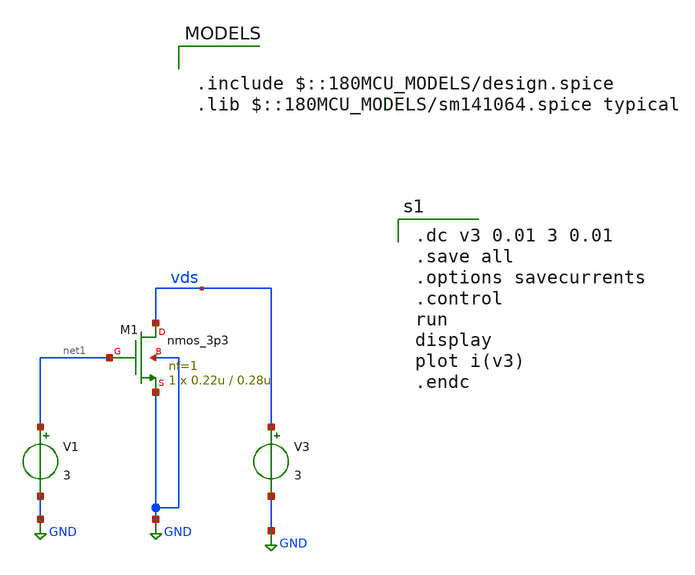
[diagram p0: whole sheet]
** sch_path: xschem/untitled-1.sch
**.subckt untitled-1
XM1 vds net1 GND GND nmos_3p3 L=0.28u W=0.22u nf=1 ad='int((nf+1)/2) * W/nf * 0.18u' as='int((nf+2)/2) * W/nf * 0.18u'
+ pd='2*int((nf+1)/2) * (W/nf + 0.18u)' ps='2*int((nf+2)/2) * (W/nf + 0.18u)' nrd='0.18u / W' nrs='0.18u / W'
+ sa=0 sb=0 sd=0 m=1
V1 net1 GND 3
V3 vds GND 3
**** begin user architecture code

.include $::180MCU_MODELS/design.spice
.lib $::180MCU_MODELS/sm141064.spice typical


.dc v3 0.01 3 0.01
.save all
.options savecurrents
.control
run
display
plot i(v3)
.endc


**** end user architecture code
**.ends
.GLOBAL GND
.end
